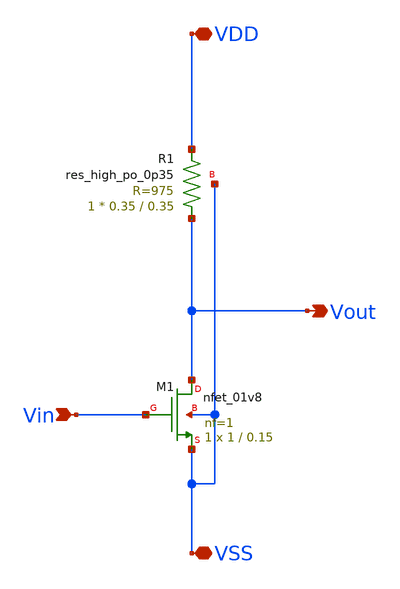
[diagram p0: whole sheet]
** sch_path: xschem/CS_Amplifier.sch
**.subckt CS_Amplifier VDD VSS Vin Vout
*.iopin VDD
*.iopin VSS
*.ipin Vin
*.opin Vout
XM1 Vout Vin VSS VSS sky130_fd_pr__nfet_01v8 L=0.15 W=1 nf=1 ad='int((nf+1)/2) * W/nf * 0.29' as='int((nf+2)/2) * W/nf * 0.29'
+ pd='2*int((nf+1)/2) * (W/nf + 0.29)' ps='2*int((nf+2)/2) * (W/nf + 0.29)' nrd='0.29 / W' nrs='0.29 / W'
+ sa=0 sb=0 sd=0 mult=1 m=1
XR1 Vout VDD VSS sky130_fd_pr__res_high_po_0p35 L=0.35 mult=1 m=1
**.ends
.end
